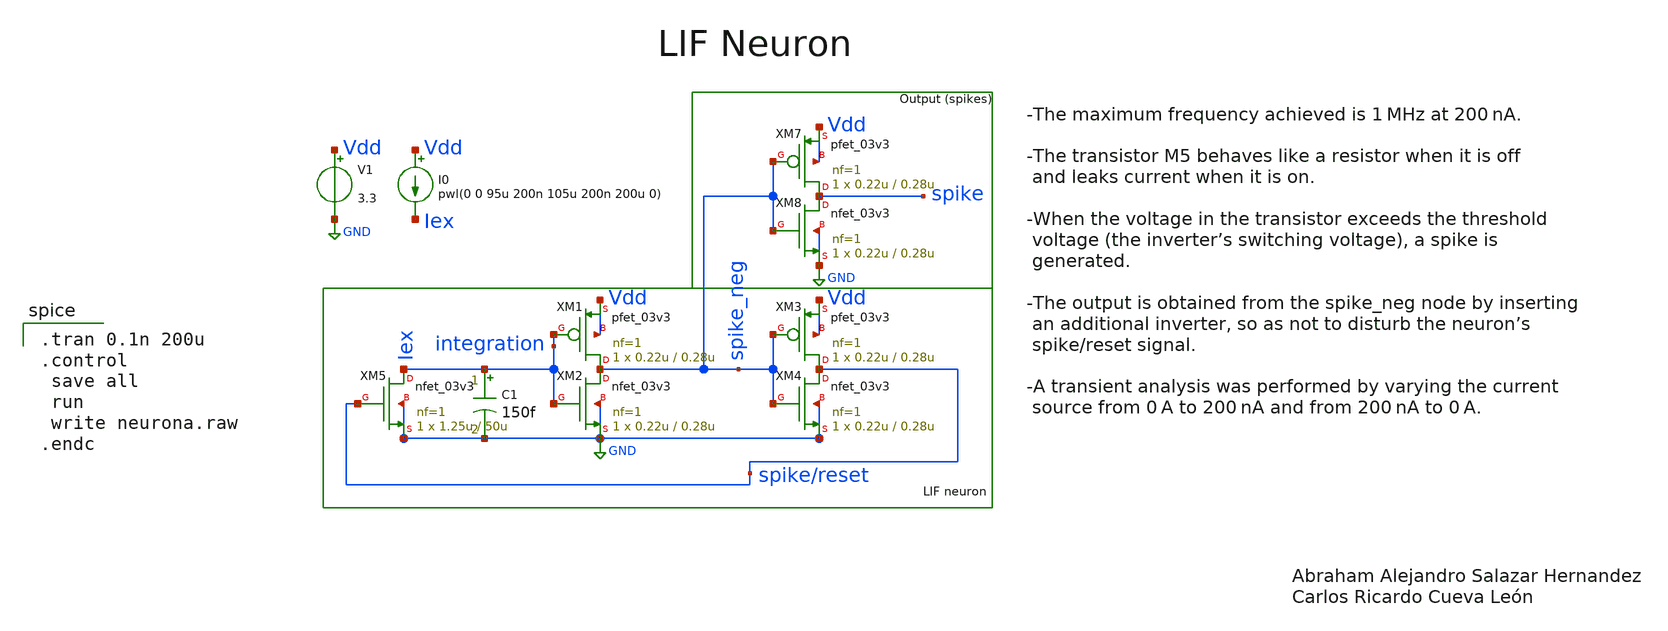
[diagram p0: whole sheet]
** sch_path: sch/lif/neurona.sch
**.subckt neurona
XM1 spike_neg Iex Vdd Vdd pfet_03v3 L=0.28u W=0.22u nf=1 ad='int((nf+1)/2) * W/nf * 0.18u' as='int((nf+2)/2) * W/nf * 0.18u'
+ pd='2*int((nf+1)/2) * (W/nf + 0.18u)' ps='2*int((nf+2)/2) * (W/nf + 0.18u)' nrd='0.18u / W' nrs='0.18u / W'
+ sa=0 sb=0 sd=0 m=1
XM2 spike_neg Iex GND GND nfet_03v3 L=0.28u W=0.22u nf=1 ad='int((nf+1)/2) * W/nf * 0.18u' as='int((nf+2)/2) * W/nf * 0.18u'
+ pd='2*int((nf+1)/2) * (W/nf + 0.18u)' ps='2*int((nf+2)/2) * (W/nf + 0.18u)' nrd='0.18u / W' nrs='0.18u / W'
+ sa=0 sb=0 sd=0 m=1
XM3 spike/reset spike_neg Vdd Vdd pfet_03v3 L=0.28u W=0.22u nf=1 ad='int((nf+1)/2) * W/nf * 0.18u' as='int((nf+2)/2) * W/nf * 0.18u'
+ pd='2*int((nf+1)/2) * (W/nf + 0.18u)' ps='2*int((nf+2)/2) * (W/nf + 0.18u)' nrd='0.18u / W' nrs='0.18u / W'
+ sa=0 sb=0 sd=0 m=1
XM4 spike/reset spike_neg GND GND nfet_03v3 L=0.28u W=0.22u nf=1 ad='int((nf+1)/2) * W/nf * 0.18u' as='int((nf+2)/2) * W/nf * 0.18u'
+ pd='2*int((nf+1)/2) * (W/nf + 0.18u)' ps='2*int((nf+2)/2) * (W/nf + 0.18u)' nrd='0.18u / W' nrs='0.18u / W'
+ sa=0 sb=0 sd=0 m=1
XM7 spike spike_neg Vdd Vdd pfet_03v3 L=0.28u W=0.22u nf=1 ad='int((nf+1)/2) * W/nf * 0.18u' as='int((nf+2)/2) * W/nf * 0.18u'
+ pd='2*int((nf+1)/2) * (W/nf + 0.18u)' ps='2*int((nf+2)/2) * (W/nf + 0.18u)' nrd='0.18u / W' nrs='0.18u / W'
+ sa=0 sb=0 sd=0 m=1
XM8 spike spike_neg GND GND nfet_03v3 L=0.28u W=0.22u nf=1 ad='int((nf+1)/2) * W/nf * 0.18u' as='int((nf+2)/2) * W/nf * 0.18u'
+ pd='2*int((nf+1)/2) * (W/nf + 0.18u)' ps='2*int((nf+2)/2) * (W/nf + 0.18u)' nrd='0.18u / W' nrs='0.18u / W'
+ sa=0 sb=0 sd=0 m=1
XM5 Iex spike/reset GND GND nfet_03v3 L=50u W=1.25u nf=1 ad='int((nf+1)/2) * W/nf * 0.18u' as='int((nf+2)/2) * W/nf * 0.18u'
+ pd='2*int((nf+1)/2) * (W/nf + 0.18u)' ps='2*int((nf+2)/2) * (W/nf + 0.18u)' nrd='0.18u / W' nrs='0.18u / W'
+ sa=0 sb=0 sd=0 m=1
V1 Vdd GND 3.3
I0 Vdd Iex pwl(0 0 95u 200n 105u 200n 200u 0)
C1 Iex GND 150f m=1
**** begin user architecture code

.include $::180MCU_MODELS/design.ngspice
.lib $::180MCU_MODELS/sm141064.ngspice typical


.tran 0.1n 200u
.control
 save all
 run
 write neurona.raw
.endc

**** end user architecture code
**.ends
.GLOBAL GND
.end
